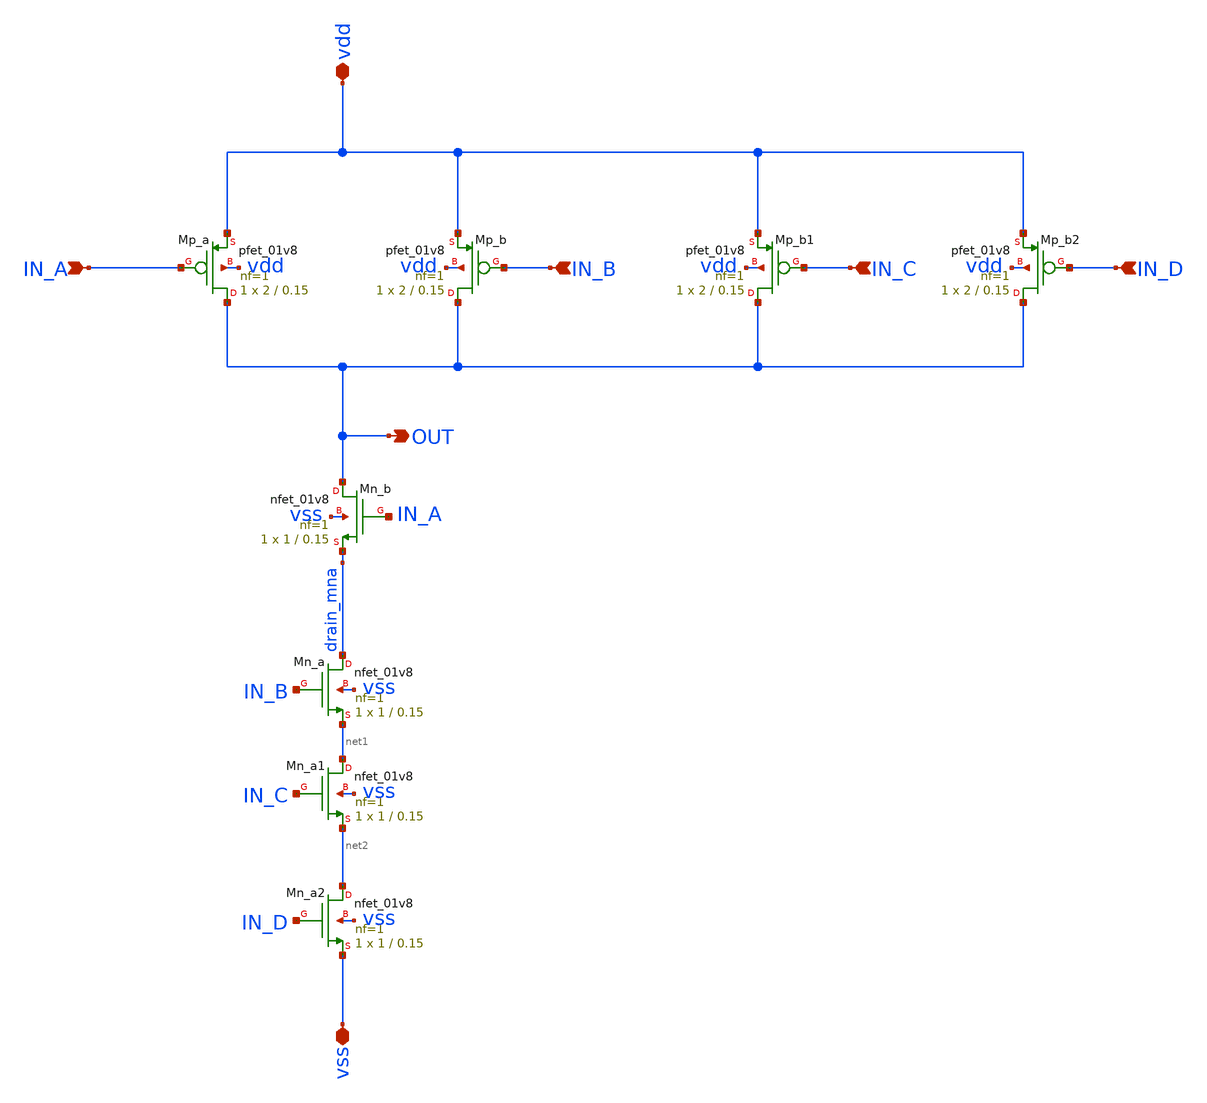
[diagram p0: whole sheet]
** sch_path: xsch/ip/logic/nand4/nand4.sch
**.subckt nand4 IN_A OUT vdd IN_B vss IN_C IN_D
*.ipin IN_A
*.opin OUT
*.iopin vdd
*.ipin IN_B
*.iopin vss
*.ipin IN_C
*.ipin IN_D
XMn_a drain_mna IN_B net1 vss sky130_fd_pr__nfet_01v8 L=0.15 W=1 nf=1 ad='int((1 + 1)/2) * 1 / 1 * 0.29'
+ as='int((1 + 2)/2) * 1 / 1 * 0.29' pd='2*int((1 + 1)/2) * (1 / 1 + 0.29)' ps='2*int((1 + 2)/2) * (1 / 1 + 0.29)'
+ nrd='0.29 / 1 ' nrs='0.29 / 1 ' sa=0 sb=0 sd=0 mult=1 m=1
XMp_a OUT IN_A vdd vdd sky130_fd_pr__pfet_01v8 L=0.15 W=2 nf=1 ad='int((nf+1)/2) * W/nf * 0.29' as='int((nf+2)/2) * W/nf * 0.29'
+ pd='2*int((nf+1)/2) * (W/nf + 0.29)' ps='2*int((nf+2)/2) * (W/nf + 0.29)' nrd='0.29 / W' nrs='0.29 / W'
+ sa=0 sb=0 sd=0 mult=1 m=1
XMp_b OUT IN_B vdd vdd sky130_fd_pr__pfet_01v8 L=0.15 W=2 nf=1 ad='int((nf+1)/2) * W/nf * 0.29' as='int((nf+2)/2) * W/nf * 0.29'
+ pd='2*int((nf+1)/2) * (W/nf + 0.29)' ps='2*int((nf+2)/2) * (W/nf + 0.29)' nrd='0.29 / W' nrs='0.29 / W'
+ sa=0 sb=0 sd=0 mult=1 m=1
XMn_b OUT IN_A drain_mna vss sky130_fd_pr__nfet_01v8 L=0.15 W=1 nf=1 ad='int((1 + 1)/2) * 1 / 1 * 0.29'
+ as='int((1 + 2)/2) * 1 / 1 * 0.29' pd='2*int((1 + 1)/2) * (1 / 1 + 0.29)' ps='2*int((1 + 2)/2) * (1 / 1 + 0.29)'
+ nrd='0.29 / 1 ' nrs='0.29 / 1 ' sa=0 sb=0 sd=0 mult=1 m=1
XMn_a1 net1 IN_C net2 vss sky130_fd_pr__nfet_01v8 L=0.15 W=1 nf=1 ad='int((1 + 1)/2) * 1 / 1 * 0.29'
+ as='int((1 + 2)/2) * 1 / 1 * 0.29' pd='2*int((1 + 1)/2) * (1 / 1 + 0.29)' ps='2*int((1 + 2)/2) * (1 / 1 + 0.29)'
+ nrd='0.29 / 1 ' nrs='0.29 / 1 ' sa=0 sb=0 sd=0 mult=1 m=1
XMp_b1 OUT IN_C vdd vdd sky130_fd_pr__pfet_01v8 L=0.15 W=2 nf=1 ad='int((nf+1)/2) * W/nf * 0.29' as='int((nf+2)/2) * W/nf * 0.29'
+ pd='2*int((nf+1)/2) * (W/nf + 0.29)' ps='2*int((nf+2)/2) * (W/nf + 0.29)' nrd='0.29 / W' nrs='0.29 / W'
+ sa=0 sb=0 sd=0 mult=1 m=1
XMp_b2 OUT IN_D vdd vdd sky130_fd_pr__pfet_01v8 L=0.15 W=2 nf=1 ad='int((nf+1)/2) * W/nf * 0.29' as='int((nf+2)/2) * W/nf * 0.29'
+ pd='2*int((nf+1)/2) * (W/nf + 0.29)' ps='2*int((nf+2)/2) * (W/nf + 0.29)' nrd='0.29 / W' nrs='0.29 / W'
+ sa=0 sb=0 sd=0 mult=1 m=1
XMn_a2 net2 IN_D vss vss sky130_fd_pr__nfet_01v8 L=0.15 W=1 nf=1 ad='int((1 + 1)/2) * 1 / 1 * 0.29' as='int((1 + 2)/2) * 1 / 1 * 0.29'
+ pd='2*int((1 + 1)/2) * (1 / 1 + 0.29)' ps='2*int((1 + 2)/2) * (1 / 1 + 0.29)' nrd='0.29 / 1 ' nrs='0.29 / 1 '
+ sa=0 sb=0 sd=0 mult=1 m=1
**.ends
.end
